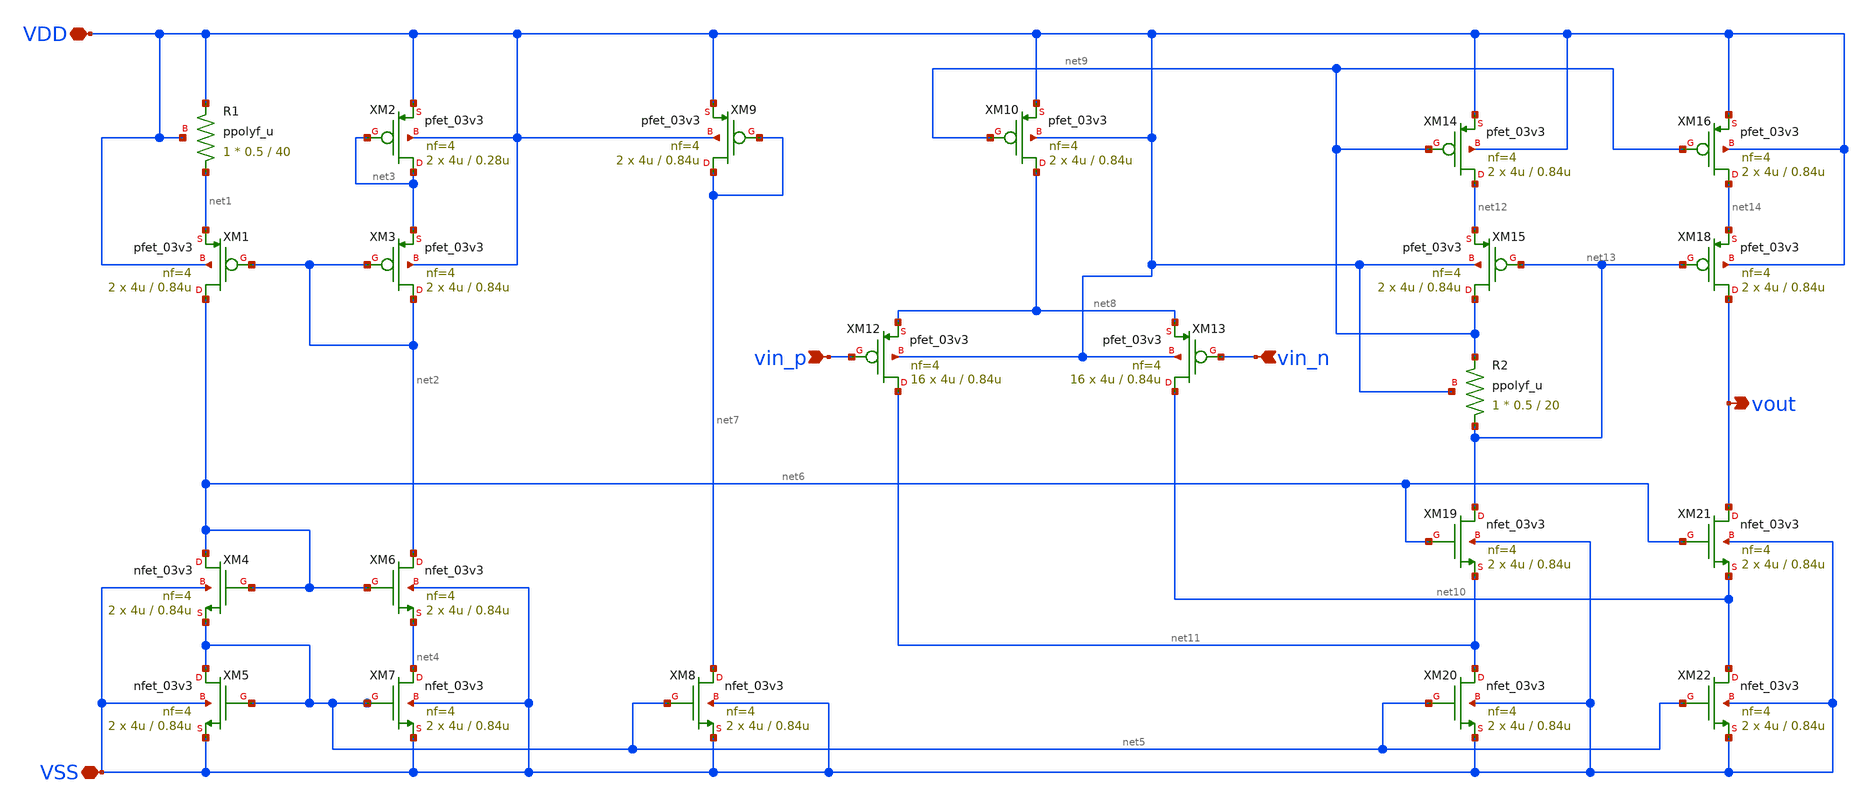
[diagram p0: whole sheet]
** sch_path: xschem/gfmcu_example_amp.sch
**.subckt gfmcu_example_amp vin_n vin_p vout VSS VDD
*.ipin vin_n
*.ipin vin_p
*.opin vout
*.iopin VSS
*.iopin VDD
XR1 net1 VDD VDD ppolyf_u r_width=0.5 r_length=40 m=1
XM1 net6 net2 net1 VDD pfet_03v3 L=0.84u W=4u nf=4 ad='int((nf+1)/2) * W/nf * 0.18u' as='int((nf+2)/2) * W/nf * 0.18u'
+ pd='2*int((nf+1)/2) * (W/nf + 0.18u)' ps='2*int((nf+2)/2) * (W/nf + 0.18u)' nrd='0.18u / W' nrs='0.18u / W'
+ sa=0 sb=0 sd=0 m=2 par=2
XM2 net3 net3 VDD VDD pfet_03v3 L=0.28u W=4u nf=4 ad='int((nf+1)/2) * W/nf * 0.18u' as='int((nf+2)/2) * W/nf * 0.18u'
+ pd='2*int((nf+1)/2) * (W/nf + 0.18u)' ps='2*int((nf+2)/2) * (W/nf + 0.18u)' nrd='0.18u / W' nrs='0.18u / W'
+ sa=0 sb=0 sd=0 m=2 par=2
XM3 net2 net2 net3 VDD pfet_03v3 L=0.84u W=4u nf=4 ad='int((nf+1)/2) * W/nf * 0.18u' as='int((nf+2)/2) * W/nf * 0.18u'
+ pd='2*int((nf+1)/2) * (W/nf + 0.18u)' ps='2*int((nf+2)/2) * (W/nf + 0.18u)' nrd='0.18u / W' nrs='0.18u / W'
+ sa=0 sb=0 sd=0 m=2 par=2
XM4 net6 net6 net5 VSS nfet_03v3 L=0.84u W=4u nf=4 ad='int((nf+1)/2) * W/nf * 0.18u' as='int((nf+2)/2) * W/nf * 0.18u'
+ pd='2*int((nf+1)/2) * (W/nf + 0.18u)' ps='2*int((nf+2)/2) * (W/nf + 0.18u)' nrd='0.18u / W' nrs='0.18u / W'
+ sa=0 sb=0 sd=0 m=2 par=2
XM5 net5 net5 VSS VSS nfet_03v3 L=0.84u W=4u nf=4 ad='int((nf+1)/2) * W/nf * 0.18u' as='int((nf+2)/2) * W/nf * 0.18u'
+ pd='2*int((nf+1)/2) * (W/nf + 0.18u)' ps='2*int((nf+2)/2) * (W/nf + 0.18u)' nrd='0.18u / W' nrs='0.18u / W'
+ sa=0 sb=0 sd=0 m=2 par=2
XM6 net2 net6 net4 VSS nfet_03v3 L=0.84u W=4u nf=4 ad='int((nf+1)/2) * W/nf * 0.18u' as='int((nf+2)/2) * W/nf * 0.18u'
+ pd='2*int((nf+1)/2) * (W/nf + 0.18u)' ps='2*int((nf+2)/2) * (W/nf + 0.18u)' nrd='0.18u / W' nrs='0.18u / W'
+ sa=0 sb=0 sd=0 m=2 par=2
XM7 net4 net5 VSS VSS nfet_03v3 L=0.84u W=4u nf=4 ad='int((nf+1)/2) * W/nf * 0.18u' as='int((nf+2)/2) * W/nf * 0.18u'
+ pd='2*int((nf+1)/2) * (W/nf + 0.18u)' ps='2*int((nf+2)/2) * (W/nf + 0.18u)' nrd='0.18u / W' nrs='0.18u / W'
+ sa=0 sb=0 sd=0 m=2 par=2
XM8 net7 net5 VSS VSS nfet_03v3 L=0.84u W=4u nf=4 ad='int((nf+1)/2) * W/nf * 0.18u' as='int((nf+2)/2) * W/nf * 0.18u'
+ pd='2*int((nf+1)/2) * (W/nf + 0.18u)' ps='2*int((nf+2)/2) * (W/nf + 0.18u)' nrd='0.18u / W' nrs='0.18u / W'
+ sa=0 sb=0 sd=0 m=2 par=2
XM9 net7 net7 VDD VDD pfet_03v3 L=0.84u W=4u nf=4 ad='int((nf+1)/2) * W/nf * 0.18u' as='int((nf+2)/2) * W/nf * 0.18u'
+ pd='2*int((nf+1)/2) * (W/nf + 0.18u)' ps='2*int((nf+2)/2) * (W/nf + 0.18u)' nrd='0.18u / W' nrs='0.18u / W'
+ sa=0 sb=0 sd=0 m=2 par=2
XM10 net8 net9 VDD VDD pfet_03v3 L=0.84u W=4u nf=4 ad='int((nf+1)/2) * W/nf * 0.18u' as='int((nf+2)/2) * W/nf * 0.18u'
+ pd='2*int((nf+1)/2) * (W/nf + 0.18u)' ps='2*int((nf+2)/2) * (W/nf + 0.18u)' nrd='0.18u / W' nrs='0.18u / W'
+ sa=0 sb=0 sd=0 m=2 par=2
XM12 net11 vin_p net8 VDD pfet_03v3 L=0.84u W=4u nf=4 ad='int((nf+1)/2) * W/nf * 0.18u' as='int((nf+2)/2) * W/nf * 0.18u'
+ pd='2*int((nf+1)/2) * (W/nf + 0.18u)' ps='2*int((nf+2)/2) * (W/nf + 0.18u)' nrd='0.18u / W' nrs='0.18u / W'
+ sa=0 sb=0 sd=0 m=16 par=16
XM13 net10 vin_n net8 VDD pfet_03v3 L=0.84u W=4u nf=4 ad='int((nf+1)/2) * W/nf * 0.18u' as='int((nf+2)/2) * W/nf * 0.18u'
+ pd='2*int((nf+1)/2) * (W/nf + 0.18u)' ps='2*int((nf+2)/2) * (W/nf + 0.18u)' nrd='0.18u / W' nrs='0.18u / W'
+ sa=0 sb=0 sd=0 m=16 par=16
XM14 net12 net9 VDD VDD pfet_03v3 L=0.84u W=4u nf=4 ad='int((nf+1)/2) * W/nf * 0.18u' as='int((nf+2)/2) * W/nf * 0.18u'
+ pd='2*int((nf+1)/2) * (W/nf + 0.18u)' ps='2*int((nf+2)/2) * (W/nf + 0.18u)' nrd='0.18u / W' nrs='0.18u / W'
+ sa=0 sb=0 sd=0 m=2 par=2
XM15 net9 net13 net12 VDD pfet_03v3 L=0.84u W=4u nf=4 ad='int((nf+1)/2) * W/nf * 0.18u' as='int((nf+2)/2) * W/nf * 0.18u'
+ pd='2*int((nf+1)/2) * (W/nf + 0.18u)' ps='2*int((nf+2)/2) * (W/nf + 0.18u)' nrd='0.18u / W' nrs='0.18u / W'
+ sa=0 sb=0 sd=0 m=2 par=2
XR2 net13 net9 VDD ppolyf_u r_width=0.5 r_length=20 m=1
XM16 net14 net9 VDD VDD pfet_03v3 L=0.84u W=4u nf=4 ad='int((nf+1)/2) * W/nf * 0.18u' as='int((nf+2)/2) * W/nf * 0.18u'
+ pd='2*int((nf+1)/2) * (W/nf + 0.18u)' ps='2*int((nf+2)/2) * (W/nf + 0.18u)' nrd='0.18u / W' nrs='0.18u / W'
+ sa=0 sb=0 sd=0 m=2 par=2
XM18 vout net13 net14 VDD pfet_03v3 L=0.84u W=4u nf=4 ad='int((nf+1)/2) * W/nf * 0.18u' as='int((nf+2)/2) * W/nf * 0.18u'
+ pd='2*int((nf+1)/2) * (W/nf + 0.18u)' ps='2*int((nf+2)/2) * (W/nf + 0.18u)' nrd='0.18u / W' nrs='0.18u / W'
+ sa=0 sb=0 sd=0 m=2 par=2
XM19 net13 net6 net11 VSS nfet_03v3 L=0.84u W=4u nf=4 ad='int((nf+1)/2) * W/nf * 0.18u' as='int((nf+2)/2) * W/nf * 0.18u'
+ pd='2*int((nf+1)/2) * (W/nf + 0.18u)' ps='2*int((nf+2)/2) * (W/nf + 0.18u)' nrd='0.18u / W' nrs='0.18u / W'
+ sa=0 sb=0 sd=0 m=2 par=2
XM20 net11 net5 VSS VSS nfet_03v3 L=0.84u W=4u nf=4 ad='int((nf+1)/2) * W/nf * 0.18u' as='int((nf+2)/2) * W/nf * 0.18u'
+ pd='2*int((nf+1)/2) * (W/nf + 0.18u)' ps='2*int((nf+2)/2) * (W/nf + 0.18u)' nrd='0.18u / W' nrs='0.18u / W'
+ sa=0 sb=0 sd=0 m=2 par=2
XM21 vout net6 net10 VSS nfet_03v3 L=0.84u W=4u nf=4 ad='int((nf+1)/2) * W/nf * 0.18u' as='int((nf+2)/2) * W/nf * 0.18u'
+ pd='2*int((nf+1)/2) * (W/nf + 0.18u)' ps='2*int((nf+2)/2) * (W/nf + 0.18u)' nrd='0.18u / W' nrs='0.18u / W'
+ sa=0 sb=0 sd=0 m=2 par=2
XM22 net10 net5 VSS VSS nfet_03v3 L=0.84u W=4u nf=4 ad='int((nf+1)/2) * W/nf * 0.18u' as='int((nf+2)/2) * W/nf * 0.18u'
+ pd='2*int((nf+1)/2) * (W/nf + 0.18u)' ps='2*int((nf+2)/2) * (W/nf + 0.18u)' nrd='0.18u / W' nrs='0.18u / W'
+ sa=0 sb=0 sd=0 m=2 par=2
**.ends
.end
